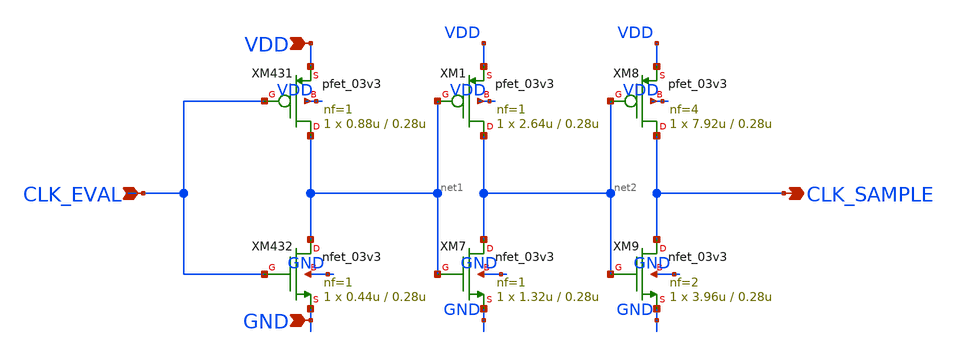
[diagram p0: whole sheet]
** sch_path: blocks/adc/encoder/sym/cascade_inv.sch
**.subckt cascade_inv VDD GND CLK_EVAL CLK_SAMPLE
*.ipin VDD
*.ipin GND
*.ipin CLK_EVAL
*.opin CLK_SAMPLE
XM431 net1 CLK_EVAL VDD VDD pfet_03v3 L=0.28u W=0.88u nf=1 ad='int((nf+1)/2) * W/nf * 0.18u' as='int((nf+2)/2) * W/nf * 0.18u'
+ pd='2*int((nf+1)/2) * (W/nf + 0.18u)' ps='2*int((nf+2)/2) * (W/nf + 0.18u)' nrd='0.18u / W' nrs='0.18u / W'
+ sa=0 sb=0 sd=0 m=1
XM432 net1 CLK_EVAL GND GND nfet_03v3 L=0.28u W=0.44u nf=1 ad='int((nf+1)/2) * W/nf * 0.18u' as='int((nf+2)/2) * W/nf * 0.18u'
+ pd='2*int((nf+1)/2) * (W/nf + 0.18u)' ps='2*int((nf+2)/2) * (W/nf + 0.18u)' nrd='0.18u / W' nrs='0.18u / W'
+ sa=0 sb=0 sd=0 m=1
XM1 net2 net1 VDD VDD pfet_03v3 L=0.28u W=2.64u nf=1 ad='int((nf+1)/2) * W/nf * 0.18u' as='int((nf+2)/2) * W/nf * 0.18u'
+ pd='2*int((nf+1)/2) * (W/nf + 0.18u)' ps='2*int((nf+2)/2) * (W/nf + 0.18u)' nrd='0.18u / W' nrs='0.18u / W'
+ sa=0 sb=0 sd=0 m=1
XM7 net2 net1 GND GND nfet_03v3 L=0.28u W=1.32u nf=1 ad='int((nf+1)/2) * W/nf * 0.18u' as='int((nf+2)/2) * W/nf * 0.18u'
+ pd='2*int((nf+1)/2) * (W/nf + 0.18u)' ps='2*int((nf+2)/2) * (W/nf + 0.18u)' nrd='0.18u / W' nrs='0.18u / W'
+ sa=0 sb=0 sd=0 m=1
XM8 CLK_SAMPLE net2 VDD VDD pfet_03v3 L=0.28u W=7.92u nf=4 ad='int((nf+1)/2) * W/nf * 0.18u' as='int((nf+2)/2) * W/nf * 0.18u'
+ pd='2*int((nf+1)/2) * (W/nf + 0.18u)' ps='2*int((nf+2)/2) * (W/nf + 0.18u)' nrd='0.18u / W' nrs='0.18u / W'
+ sa=0 sb=0 sd=0 m=1
XM9 CLK_SAMPLE net2 GND GND nfet_03v3 L=0.28u W=3.96u nf=2 ad='int((nf+1)/2) * W/nf * 0.18u' as='int((nf+2)/2) * W/nf * 0.18u'
+ pd='2*int((nf+1)/2) * (W/nf + 0.18u)' ps='2*int((nf+2)/2) * (W/nf + 0.18u)' nrd='0.18u / W' nrs='0.18u / W'
+ sa=0 sb=0 sd=0 m=1
**.ends
.end
